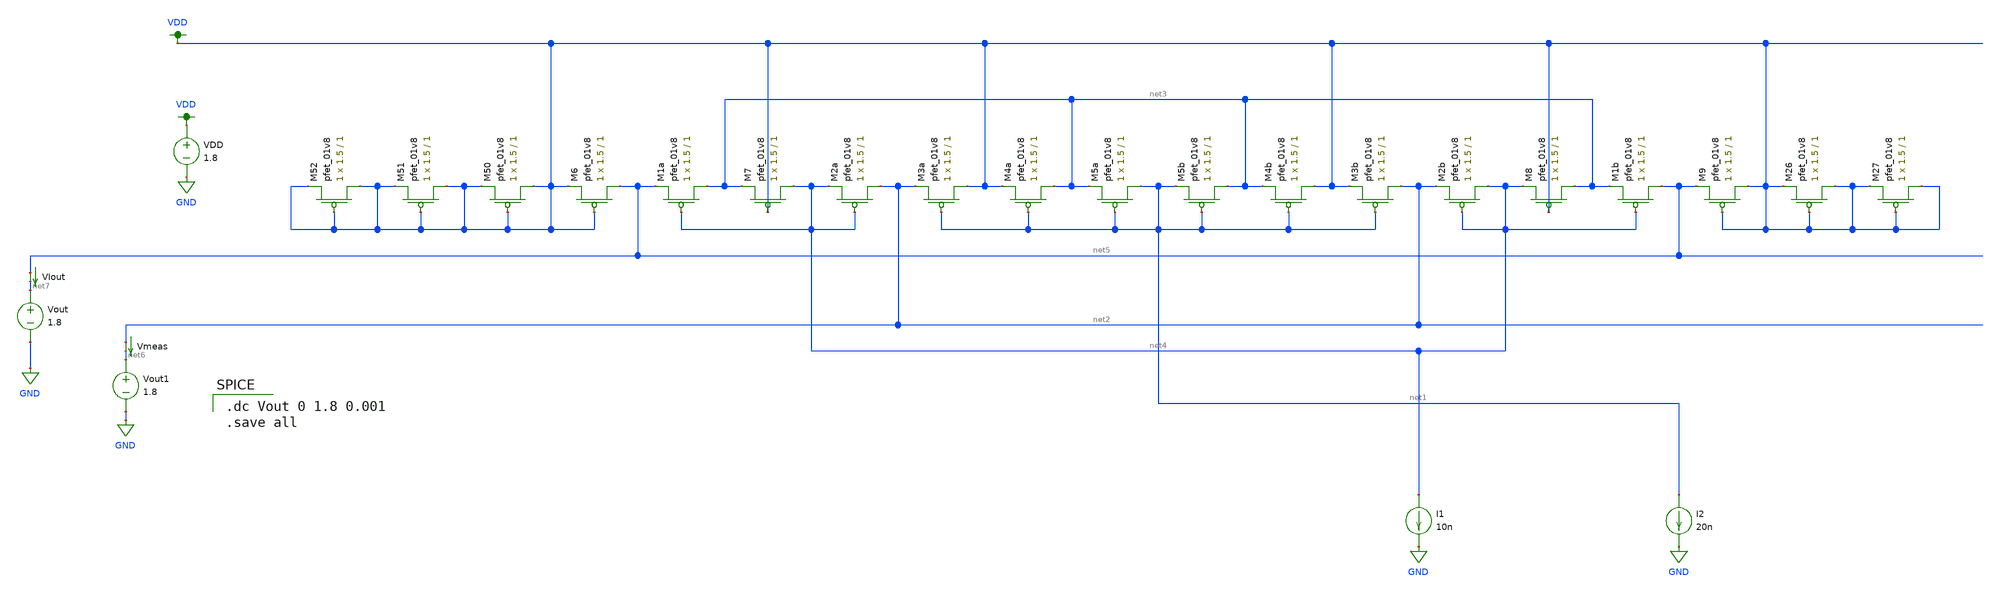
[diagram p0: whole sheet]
** sch_path: schematic/LDS/test/low-voltage_super-wilson-test.sch
**.subckt low-voltage_super-wilson-test
XM7 net4 VDD net3 VDD sky130_fd_pr__pfet_01v8 L=1 W=1.5 nf=1 ad='int((nf+1)/2) * W/nf * 0.29' as='int((nf+2)/2) * W/nf * 0.29'
+ pd='2*int((nf+1)/2) * (W/nf + 0.29)' ps='2*int((nf+2)/2) * (W/nf + 0.29)' nrd='0.29 / W' nrs='0.29 / W'
+ sa=0 sb=0 sd=0 mult=1 m=1
XM2a net2 net4 net4 VDD sky130_fd_pr__pfet_01v8 L=1 W=1.5 nf=1 ad='int((nf+1)/2) * W/nf * 0.29' as='int((nf+2)/2) * W/nf * 0.29'
+ pd='2*int((nf+1)/2) * (W/nf + 0.29)' ps='2*int((nf+2)/2) * (W/nf + 0.29)' nrd='0.29 / W' nrs='0.29 / W'
+ sa=0 sb=0 sd=0 mult=1 m=1
XM3a VDD net1 net2 VDD sky130_fd_pr__pfet_01v8 L=1 W=1.5 nf=1 ad='int((nf+1)/2) * W/nf * 0.29' as='int((nf+2)/2) * W/nf * 0.29'
+ pd='2*int((nf+1)/2) * (W/nf + 0.29)' ps='2*int((nf+2)/2) * (W/nf + 0.29)' nrd='0.29 / W' nrs='0.29 / W'
+ sa=0 sb=0 sd=0 mult=1 m=1
XM4a net3 net1 VDD VDD sky130_fd_pr__pfet_01v8 L=1 W=1.5 nf=1 ad='int((nf+1)/2) * W/nf * 0.29' as='int((nf+2)/2) * W/nf * 0.29'
+ pd='2*int((nf+1)/2) * (W/nf + 0.29)' ps='2*int((nf+2)/2) * (W/nf + 0.29)' nrd='0.29 / W' nrs='0.29 / W'
+ sa=0 sb=0 sd=0 mult=1 m=1
XM5a net1 net1 net3 VDD sky130_fd_pr__pfet_01v8 L=1 W=1.5 nf=1 ad='int((nf+1)/2) * W/nf * 0.29' as='int((nf+2)/2) * W/nf * 0.29'
+ pd='2*int((nf+1)/2) * (W/nf + 0.29)' ps='2*int((nf+2)/2) * (W/nf + 0.29)' nrd='0.29 / W' nrs='0.29 / W'
+ sa=0 sb=0 sd=0 mult=1 m=1
XM5b net3 net1 net1 VDD sky130_fd_pr__pfet_01v8 L=1 W=1.5 nf=1 ad='int((nf+1)/2) * W/nf * 0.29' as='int((nf+2)/2) * W/nf * 0.29'
+ pd='2*int((nf+1)/2) * (W/nf + 0.29)' ps='2*int((nf+2)/2) * (W/nf + 0.29)' nrd='0.29 / W' nrs='0.29 / W'
+ sa=0 sb=0 sd=0 mult=1 m=1
XM4b VDD net1 net3 VDD sky130_fd_pr__pfet_01v8 L=1 W=1.5 nf=1 ad='int((nf+1)/2) * W/nf * 0.29' as='int((nf+2)/2) * W/nf * 0.29'
+ pd='2*int((nf+1)/2) * (W/nf + 0.29)' ps='2*int((nf+2)/2) * (W/nf + 0.29)' nrd='0.29 / W' nrs='0.29 / W'
+ sa=0 sb=0 sd=0 mult=1 m=1
XM3b net2 net1 VDD VDD sky130_fd_pr__pfet_01v8 L=1 W=1.5 nf=1 ad='int((nf+1)/2) * W/nf * 0.29' as='int((nf+2)/2) * W/nf * 0.29'
+ pd='2*int((nf+1)/2) * (W/nf + 0.29)' ps='2*int((nf+2)/2) * (W/nf + 0.29)' nrd='0.29 / W' nrs='0.29 / W'
+ sa=0 sb=0 sd=0 mult=1 m=1
XM2b net4 net4 net2 VDD sky130_fd_pr__pfet_01v8 L=1 W=1.5 nf=1 ad='int((nf+1)/2) * W/nf * 0.29' as='int((nf+2)/2) * W/nf * 0.29'
+ pd='2*int((nf+1)/2) * (W/nf + 0.29)' ps='2*int((nf+2)/2) * (W/nf + 0.29)' nrd='0.29 / W' nrs='0.29 / W'
+ sa=0 sb=0 sd=0 mult=1 m=1
XM8 net3 VDD net4 VDD sky130_fd_pr__pfet_01v8 L=1 W=1.5 nf=1 ad='int((nf+1)/2) * W/nf * 0.29' as='int((nf+2)/2) * W/nf * 0.29'
+ pd='2*int((nf+1)/2) * (W/nf + 0.29)' ps='2*int((nf+2)/2) * (W/nf + 0.29)' nrd='0.29 / W' nrs='0.29 / W'
+ sa=0 sb=0 sd=0 mult=1 m=1
XM1a net3 net4 net5 VDD sky130_fd_pr__pfet_01v8 L=1 W=1.5 nf=1 ad='int((nf+1)/2) * W/nf * 0.29' as='int((nf+2)/2) * W/nf * 0.29'
+ pd='2*int((nf+1)/2) * (W/nf + 0.29)' ps='2*int((nf+2)/2) * (W/nf + 0.29)' nrd='0.29 / W' nrs='0.29 / W'
+ sa=0 sb=0 sd=0 mult=1 m=1
XM1b net5 net4 net3 VDD sky130_fd_pr__pfet_01v8 L=1 W=1.5 nf=1 ad='int((nf+1)/2) * W/nf * 0.29' as='int((nf+2)/2) * W/nf * 0.29'
+ pd='2*int((nf+1)/2) * (W/nf + 0.29)' ps='2*int((nf+2)/2) * (W/nf + 0.29)' nrd='0.29 / W' nrs='0.29 / W'
+ sa=0 sb=0 sd=0 mult=1 m=1
XM6 net5 VDD VDD VDD sky130_fd_pr__pfet_01v8 L=1 W=1.5 nf=1 ad='int((nf+1)/2) * W/nf * 0.29' as='int((nf+2)/2) * W/nf * 0.29'
+ pd='2*int((nf+1)/2) * (W/nf + 0.29)' ps='2*int((nf+2)/2) * (W/nf + 0.29)' nrd='0.29 / W' nrs='0.29 / W'
+ sa=0 sb=0 sd=0 mult=1 m=1
XM9 VDD VDD net5 VDD sky130_fd_pr__pfet_01v8 L=1 W=1.5 nf=1 ad='int((nf+1)/2) * W/nf * 0.29' as='int((nf+2)/2) * W/nf * 0.29'
+ pd='2*int((nf+1)/2) * (W/nf + 0.29)' ps='2*int((nf+2)/2) * (W/nf + 0.29)' nrd='0.29 / W' nrs='0.29 / W'
+ sa=0 sb=0 sd=0 mult=1 m=1
XM26 VDD VDD VDD VDD sky130_fd_pr__pfet_01v8 L=1 W=1.5 nf=1 ad='int((nf+1)/2) * W/nf * 0.29' as='int((nf+2)/2) * W/nf * 0.29'
+ pd='2*int((nf+1)/2) * (W/nf + 0.29)' ps='2*int((nf+2)/2) * (W/nf + 0.29)' nrd='0.29 / W' nrs='0.29 / W'
+ sa=0 sb=0 sd=0 mult=1 m=1
XM27 VDD VDD VDD VDD sky130_fd_pr__pfet_01v8 L=1 W=1.5 nf=1 ad='int((nf+1)/2) * W/nf * 0.29' as='int((nf+2)/2) * W/nf * 0.29'
+ pd='2*int((nf+1)/2) * (W/nf + 0.29)' ps='2*int((nf+2)/2) * (W/nf + 0.29)' nrd='0.29 / W' nrs='0.29 / W'
+ sa=0 sb=0 sd=0 mult=1 m=1
XM50 VDD VDD VDD VDD sky130_fd_pr__pfet_01v8 L=1 W=1.5 nf=1 ad='int((nf+1)/2) * W/nf * 0.29' as='int((nf+2)/2) * W/nf * 0.29'
+ pd='2*int((nf+1)/2) * (W/nf + 0.29)' ps='2*int((nf+2)/2) * (W/nf + 0.29)' nrd='0.29 / W' nrs='0.29 / W'
+ sa=0 sb=0 sd=0 mult=1 m=1
XM51 VDD VDD VDD VDD sky130_fd_pr__pfet_01v8 L=1 W=1.5 nf=1 ad='int((nf+1)/2) * W/nf * 0.29' as='int((nf+2)/2) * W/nf * 0.29'
+ pd='2*int((nf+1)/2) * (W/nf + 0.29)' ps='2*int((nf+2)/2) * (W/nf + 0.29)' nrd='0.29 / W' nrs='0.29 / W'
+ sa=0 sb=0 sd=0 mult=1 m=1
XM52 VDD VDD VDD VDD sky130_fd_pr__pfet_01v8 L=1 W=1.5 nf=1 ad='int((nf+1)/2) * W/nf * 0.29' as='int((nf+2)/2) * W/nf * 0.29'
+ pd='2*int((nf+1)/2) * (W/nf + 0.29)' ps='2*int((nf+2)/2) * (W/nf + 0.29)' nrd='0.29 / W' nrs='0.29 / W'
+ sa=0 sb=0 sd=0 mult=1 m=1
VDD VDD GND 1.8
I1 net4 GND 10n
I2 net1 GND 20n
Vmeas net2 net6 0
.save i(vmeas)
Vout net7 GND 1.8
VIout net5 net7 0
.save i(viout)
Vout1 net6 GND 1.8
**** begin user architecture code

.option wnflag=1
.param MC_SWITCH=0.0
.lib ~/skywater/skywater-pdk/libraries/sky130_fd_pr_ngspice/latest/models/sky130.lib.spice tt


.dc Vout 0 1.8 0.001
.save all

**** end user architecture code
**.ends
.GLOBAL VDD
.GLOBAL GND
.end
